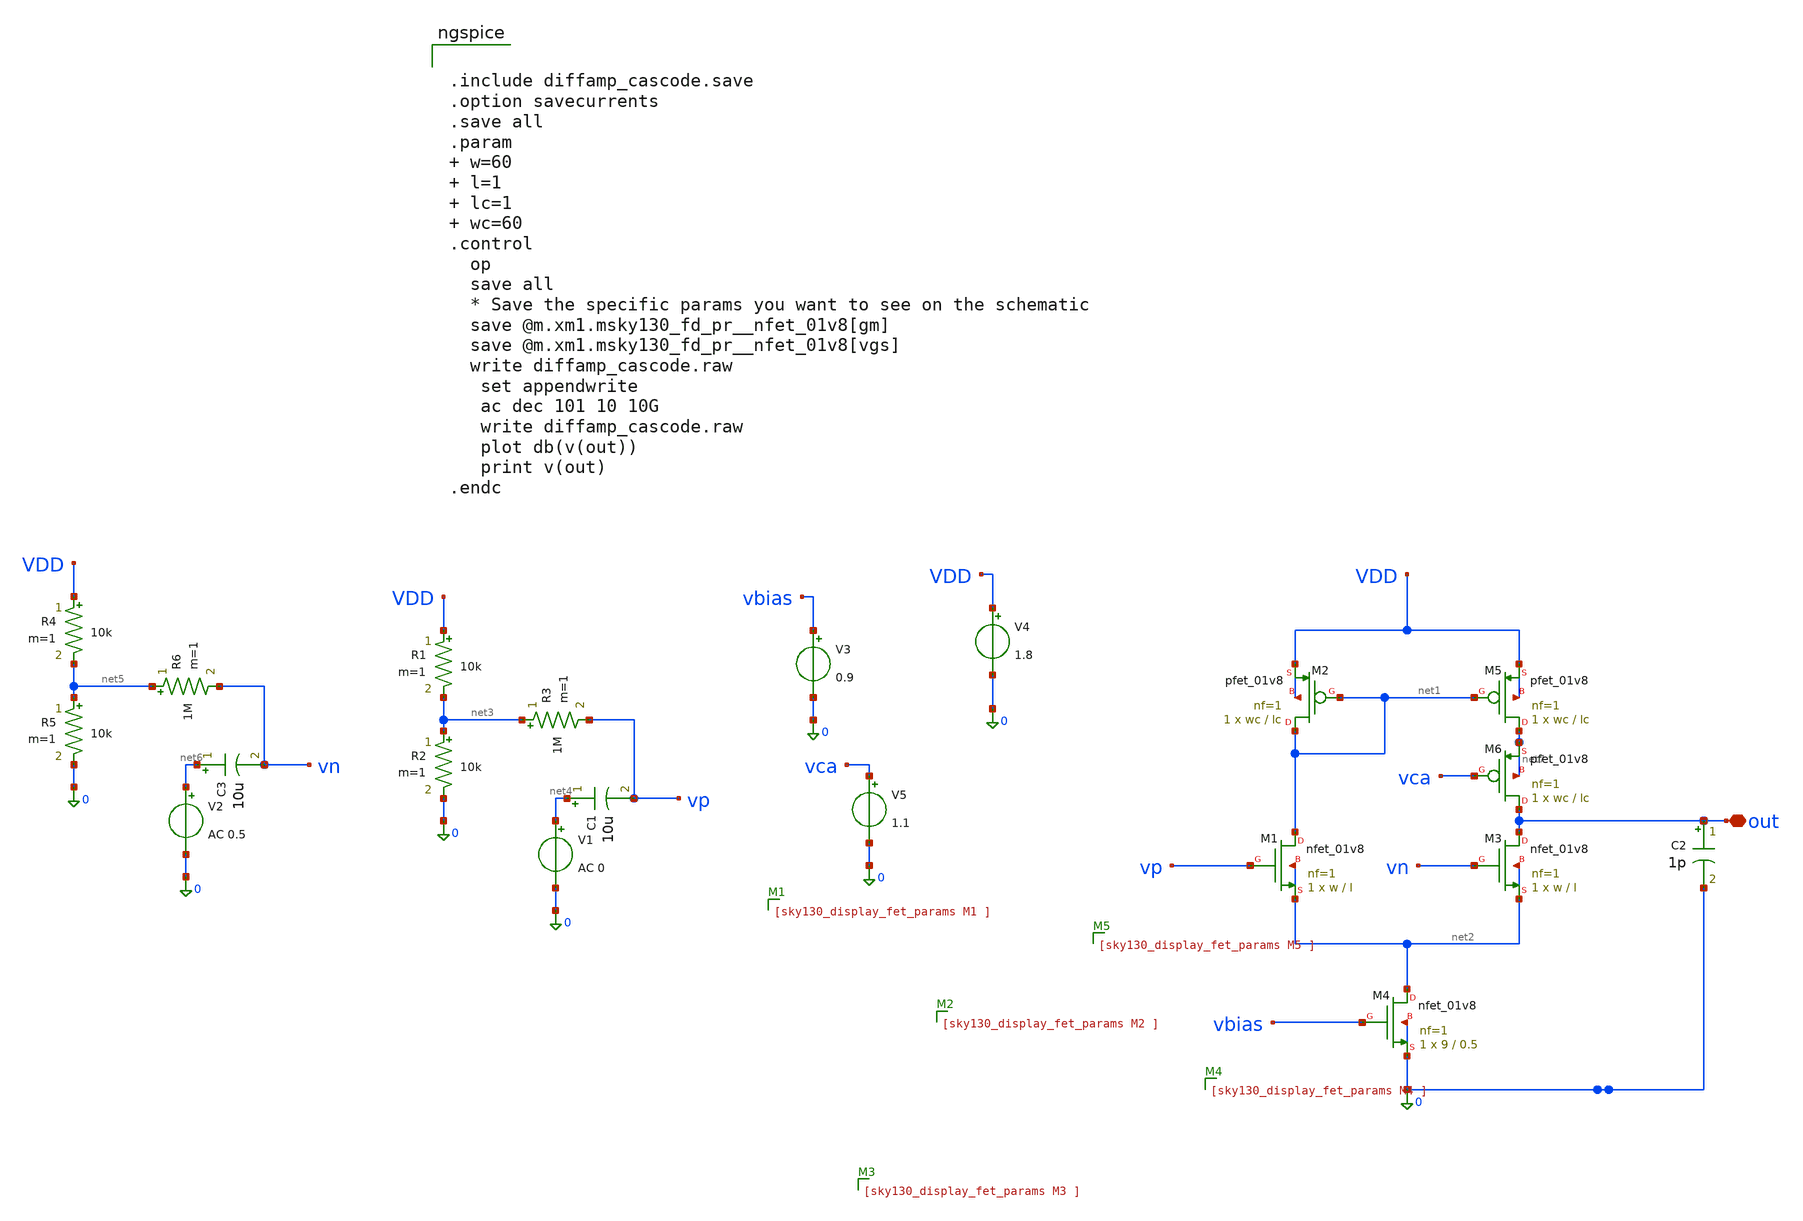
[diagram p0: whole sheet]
** sch_path: design_data/xschem/diffamp_cascode.sch
**.subckt diffamp_cascode out
*.iopin out
XM2 net1 net1 VDD VDD sky130_fd_pr__pfet_01v8 L=lc W=wc nf=1 ad='int((1 + 1)/2) * wc / 1 * 0.29' as='int((1 + 2)/2) * wc / 1 * 0.29'
+ pd='2*int((1 + 1)/2) * (wc / 1 + 0.29)' ps='2*int((1 + 2)/2) * (wc / 1 + 0.29)' nrd='0.29 / wc ' nrs='0.29 / wc '
+ sa=0 sb=0 sd=0 mult=1 m=1
XM3 out vn net2 net2 sky130_fd_pr__nfet_01v8 L=l W=w nf=1 ad='int((1 + 1)/2) * w / 1 * 0.29' as='int((1 + 2)/2) * w / 1 * 0.29'
+ pd='2*int((1 + 1)/2) * (w / 1 + 0.29)' ps='2*int((1 + 2)/2) * (w / 1 + 0.29)' nrd='0.29 / w ' nrs='0.29 / w '
+ sa=0 sb=0 sd=0 mult=1 m=1
XM1 net1 vp net2 net2 sky130_fd_pr__nfet_01v8 L=l W=w nf=1 ad='int((1 + 1)/2) * w / 1 * 0.29' as='int((1 + 2)/2) * w / 1 * 0.29'
+ pd='2*int((1 + 1)/2) * (w / 1 + 0.29)' ps='2*int((1 + 2)/2) * (w / 1 + 0.29)' nrd='0.29 / w ' nrs='0.29 / w '
+ sa=0 sb=0 sd=0 mult=1 m=1
XM4 net2 vbias 0 0 sky130_fd_pr__nfet_01v8 L=0.5 W=9 nf=1 ad='int((1 + 1)/2) * 9 / 1 * 0.29' as='int((1 + 2)/2) * 9 / 1 * 0.29'
+ pd='2*int((1 + 1)/2) * (9 / 1 + 0.29)' ps='2*int((1 + 2)/2) * (9 / 1 + 0.29)' nrd='0.29 / 9 ' nrs='0.29 / 9 '
+ sa=0 sb=0 sd=0 mult=1 m=1
XM5 net7 net1 VDD VDD sky130_fd_pr__pfet_01v8 L=lc W=wc nf=1 ad='int((1 + 1)/2) * wc / 1 * 0.29' as='int((1 + 2)/2) * wc / 1 * 0.29'
+ pd='2*int((1 + 1)/2) * (wc / 1 + 0.29)' ps='2*int((1 + 2)/2) * (wc / 1 + 0.29)' nrd='0.29 / wc ' nrs='0.29 / wc '
+ sa=0 sb=0 sd=0 mult=1 m=1
V1 net4 0 AC 0
R1 VDD net3 10k m=1
R2 net3 0 10k m=1
R3 net3 vp 1M m=1
C1 net4 vp 10u m=1
C2 out 0 1p m=1
V2 net6 0 AC 0.5
R4 VDD net5 10k m=1
R5 net5 0 10k m=1
R6 net5 vn 1M m=1
C3 net6 vn 10u m=1
V3 vbias 0 0.9
V4 VDD 0 1.8
XM6 out vca net7 net7 sky130_fd_pr__pfet_01v8 L=lc W=wc nf=1 ad='int((1 + 1)/2) * wc / 1 * 0.29' as='int((1 + 2)/2) * wc / 1 * 0.29'
+ pd='2*int((1 + 1)/2) * (wc / 1 + 0.29)' ps='2*int((1 + 2)/2) * (wc / 1 + 0.29)' nrd='0.29 / wc ' nrs='0.29 / wc '
+ sa=0 sb=0 sd=0 mult=1 m=1
V5 vca 0 1.1
**** begin user architecture code


.include diffamp_cascode.save
.option savecurrents
.save all
.param  w=60  l=1  lc=1  wc=60
.control
  op
  save all
  * Save the specific params you want to see on the schematic
  save @m.xm1.msky130_fd_pr__nfet_01v8[gm]
  save @m.xm1.msky130_fd_pr__nfet_01v8[vgs]
  write diffamp_cascode.raw
   set appendwrite
   ac dec 101 10 10G
   write diffamp_cascode.raw
   plot db(v(out))
   print v(out)
.endc



** opencircuitdesign pdks install
.lib $::SKYWATER_MODELS/sky130.lib.spice tt

**** end user architecture code
**.ends
.end
